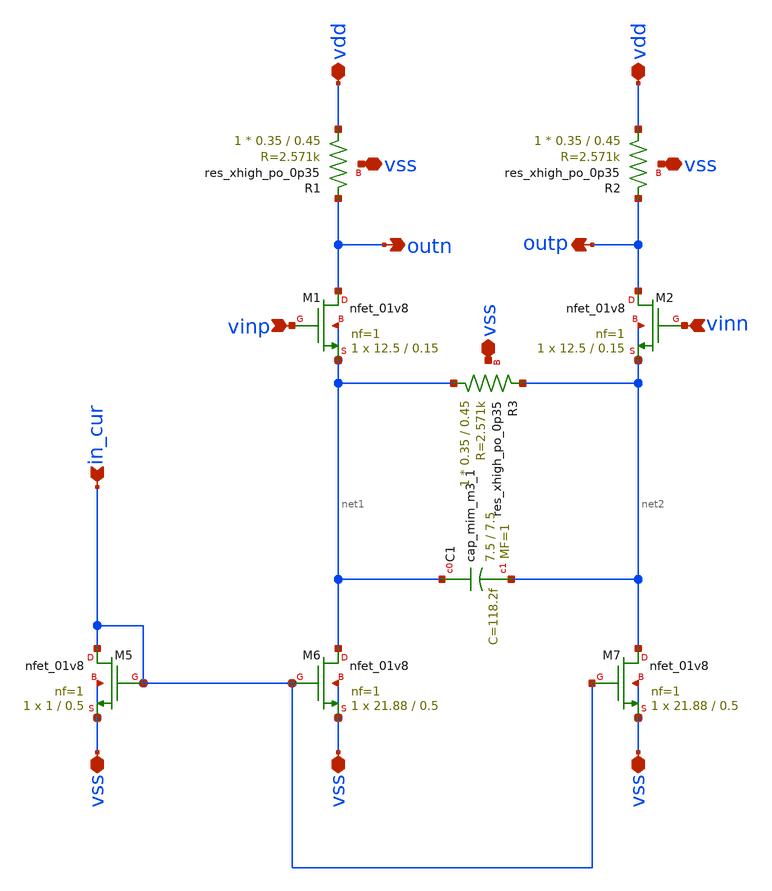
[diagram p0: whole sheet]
** sch_path: CTLE/ctle-base.sch
**.subckt ctle-base vdd vdd vss vss vss vinp vinn outn outp in_cur vss vss vss
*.iopin vdd
*.iopin vdd
*.iopin vss
*.iopin vss
*.iopin vss
*.ipin vinp
*.ipin vinn
*.opin outn
*.opin outp
*.ipin in_cur
*.iopin vss
*.iopin vss
*.iopin vss
XM1 outn vinp net1 net1 sky130_fd_pr__nfet_01v8 L=0.15 W=12.5 nf=1 ad='int((nf+1)/2) * W/nf * 0.29' as='int((nf+2)/2) * W/nf * 0.29'
+ pd='2*int((nf+1)/2) * (W/nf + 0.29)' ps='2*int((nf+2)/2) * (W/nf + 0.29)' nrd='0.29 / W' nrs='0.29 / W'
+ sa=0 sb=0 sd=0 mult=1 m=1
XM2 outp vinn net2 net2 sky130_fd_pr__nfet_01v8 L=0.15 W=12.5 nf=1 ad='int((nf+1)/2) * W/nf * 0.29' as='int((nf+2)/2) * W/nf * 0.29'
+ pd='2*int((nf+1)/2) * (W/nf + 0.29)' ps='2*int((nf+2)/2) * (W/nf + 0.29)' nrd='0.29 / W' nrs='0.29 / W'
+ sa=0 sb=0 sd=0 mult=1 m=1
XC1 net1 net2 sky130_fd_pr__cap_mim_m3_1 W=7.5 L=7.5 MF=1 m=1
XM5 in_cur in_cur vss vss sky130_fd_pr__nfet_01v8 L=0.5 W=1 nf=1 ad='int((nf+1)/2) * W/nf * 0.29' as='int((nf+2)/2) * W/nf * 0.29'
+ pd='2*int((nf+1)/2) * (W/nf + 0.29)' ps='2*int((nf+2)/2) * (W/nf + 0.29)' nrd='0.29 / W' nrs='0.29 / W'
+ sa=0 sb=0 sd=0 mult=1 m=1
XM6 net1 in_cur vss vss sky130_fd_pr__nfet_01v8 L=0.5 W=21.88 nf=1 ad='int((nf+1)/2) * W/nf * 0.29' as='int((nf+2)/2) * W/nf * 0.29'
+ pd='2*int((nf+1)/2) * (W/nf + 0.29)' ps='2*int((nf+2)/2) * (W/nf + 0.29)' nrd='0.29 / W' nrs='0.29 / W'
+ sa=0 sb=0 sd=0 mult=1 m=1
XM7 net2 in_cur vss vss sky130_fd_pr__nfet_01v8 L=0.5 W=21.88 nf=1 ad='int((nf+1)/2) * W/nf * 0.29' as='int((nf+2)/2) * W/nf * 0.29'
+ pd='2*int((nf+1)/2) * (W/nf + 0.29)' ps='2*int((nf+2)/2) * (W/nf + 0.29)' nrd='0.29 / W' nrs='0.29 / W'
+ sa=0 sb=0 sd=0 mult=1 m=1
XR3 net1 net2 vss sky130_fd_pr__res_xhigh_po_0p35 L=0.45 mult=1 m=1
XR1 vdd outn vss sky130_fd_pr__res_xhigh_po_0p35 L=0.45 mult=1 m=1
XR2 vdd outp vss sky130_fd_pr__res_xhigh_po_0p35 L=0.45 mult=1 m=1
**.ends
.end
